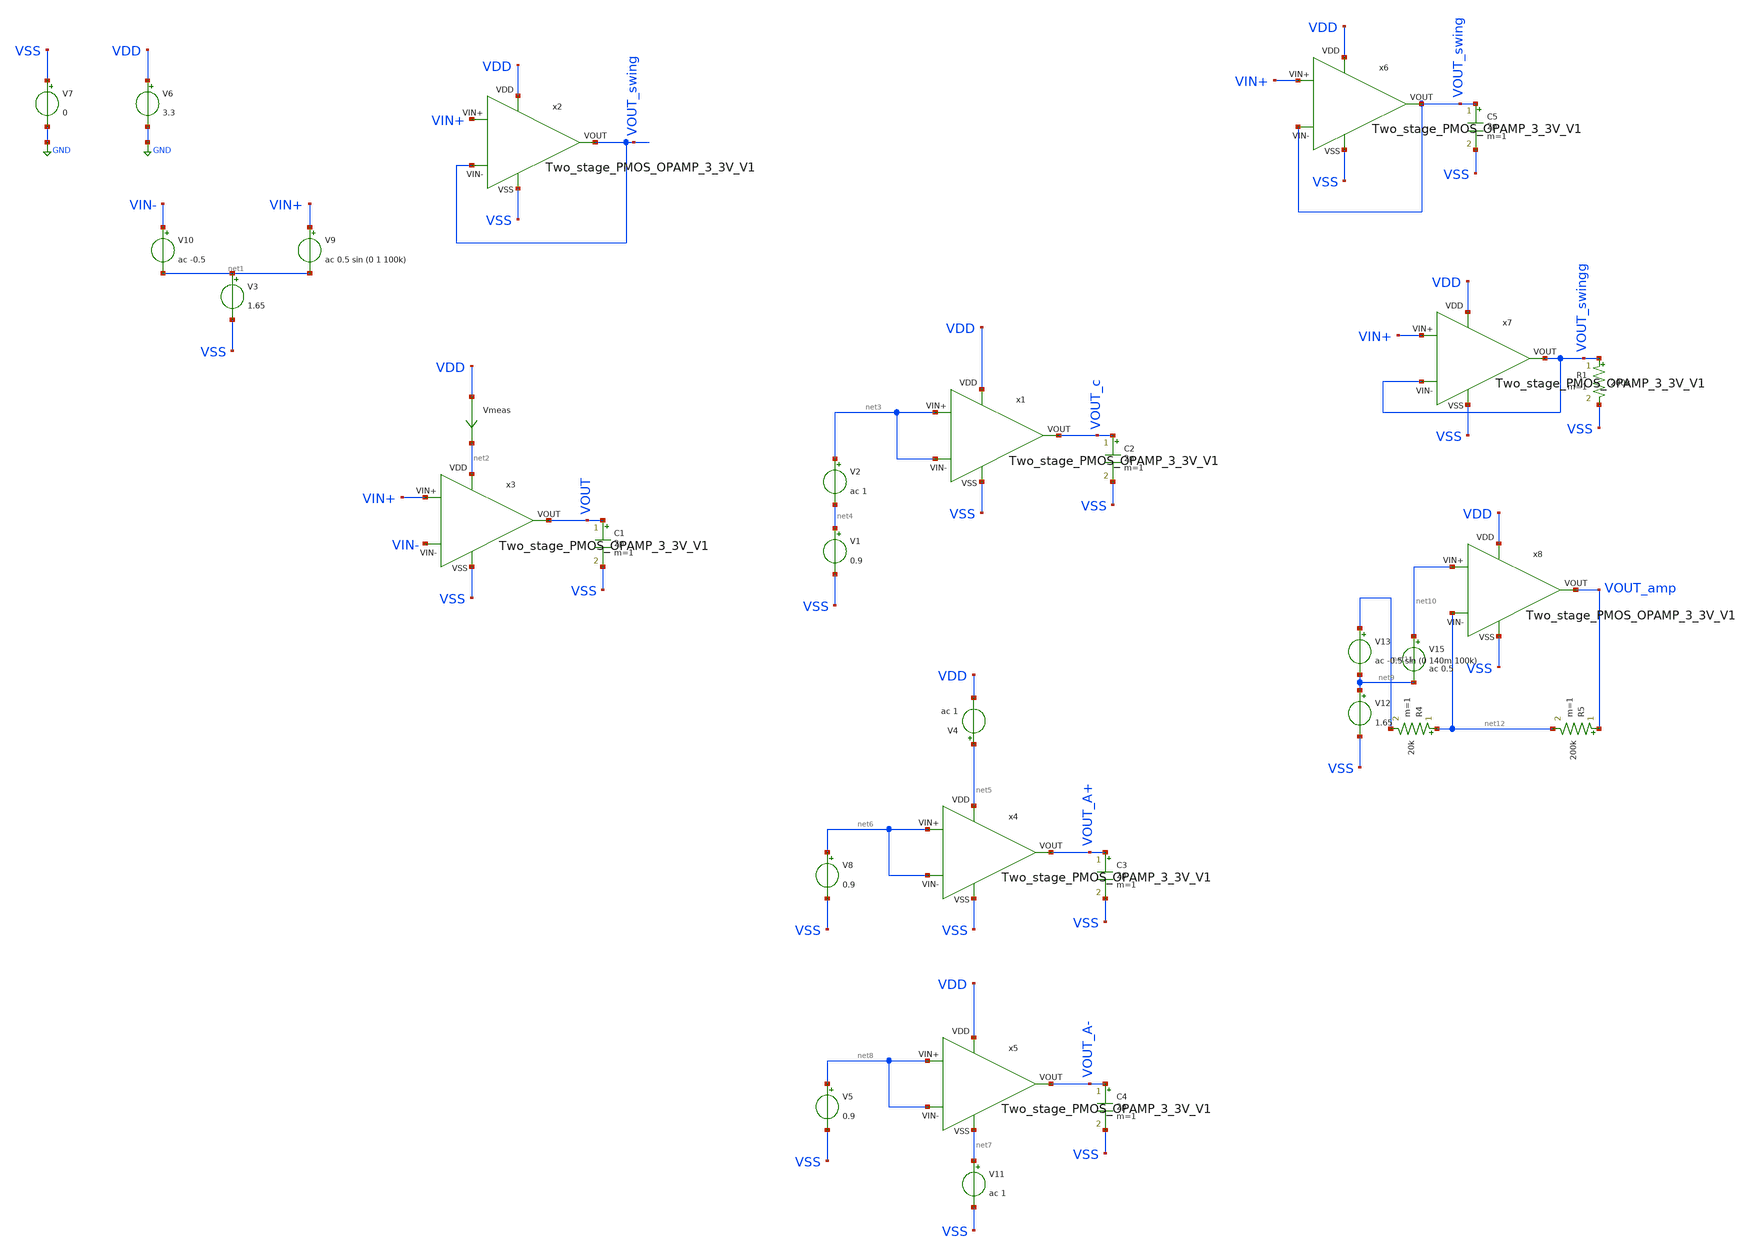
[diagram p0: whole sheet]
** sch_path: my_ip/gf180mcuD/Two_stage_PMOS_OPAMP_3_3V_V1/testbench.sch
**.subckt testbench
V6 VDD GND 3.3
V7 VSS GND 0
V3 net1 VSS 1.65
V9 VIN+ net1 ac 0.5 sin (0 1 100k)
V10 VIN- net1 ac -0.5
x2 VDD VSS VOUT_swing VIN+ VOUT_swing Two_stage_PMOS_OPAMP_3_3V_V1
C1 VOUT VSS 2p m=1
Vmeas VDD net2 0
.save i(vmeas)
x3 net2 VSS VIN- VIN+ VOUT Two_stage_PMOS_OPAMP_3_3V_V1
C2 VOUT_c VSS 2p m=1
V1 net4 VSS 0.9
V2 net3 net4 ac 1
C3 VOUT_A+ VSS 2p m=1
V8 net6 VSS 0.9
V4 net5 VDD ac 1
C4 VOUT_A- VSS 2p m=1
V5 net8 VSS 0.9
V11 net7 VSS ac 1
x1 VDD VSS net3 net3 VOUT_c Two_stage_PMOS_OPAMP_3_3V_V1
x4 net5 VSS net6 net6 VOUT_A+ Two_stage_PMOS_OPAMP_3_3V_V1
x5 VDD net7 net8 net8 VOUT_A- Two_stage_PMOS_OPAMP_3_3V_V1
C5 VOUT_swing VSS 2p m=1
R1 VOUT_swingg VSS 200k m=1
V12 net9 VSS 1.65
V13 net11 net9 ac -0.5 sin (0 140m 100k)
x6 VDD VSS VOUT_swing VIN+ VOUT_swing Two_stage_PMOS_OPAMP_3_3V_V1
x7 VDD VSS VOUT_swingg VIN+ VOUT_swingg Two_stage_PMOS_OPAMP_3_3V_V1
x8 VDD VSS net12 net10 VOUT_amp Two_stage_PMOS_OPAMP_3_3V_V1
V15 net10 net9 ac 0.5
R4 net12 net11 20k m=1
R5 VOUT_amp net12 200k m=1
**** begin user architecture code

.include $::180MCU_MODELS/design.ngspice
.lib $::180MCU_MODELS/sm141064.ngspice typical
.lib $::180MCU_MODELS/sm141064.ngspice cap_mim
.lib $::180MCU_MODELS/sm141064.ngspice res_typical
.lib $::180MCU_MODELS/sm141064.ngspice moscap_typical
.lib $::180MCU_MODELS/sm141064.ngspice mimcap_typical
* .lib $::180MCU_MODELS/sm141064.ngspice res_statistical



.TEMP 27
.control
save all
dc V3 0 3.3 0.001
*dc simulation
plot i(Vmeas)
plot v(VOUT_1)
plot v(VOUT)
plot v(VOUT_swing)
ac dec 10 1 50G
plot db(v(VOUT)) (180*ph(v(VOUT))/pi)
plot (db(v(VOUT))-db(v(VOUT_c)))
plot (db(v(VOUT))-db(v(VOUT_A+)))
plot (db(v(VOUT))-db(v(VOUT_A-)))
plot db(v(VOUT_amp))
tran 1ns 20u
plot v(VOUT_swing) v(VIN+) v(VOUT_swingg)
plot v(VOUT_amp)
.endc

**** end user architecture code
**.ends
.GLOBAL GND
.end
